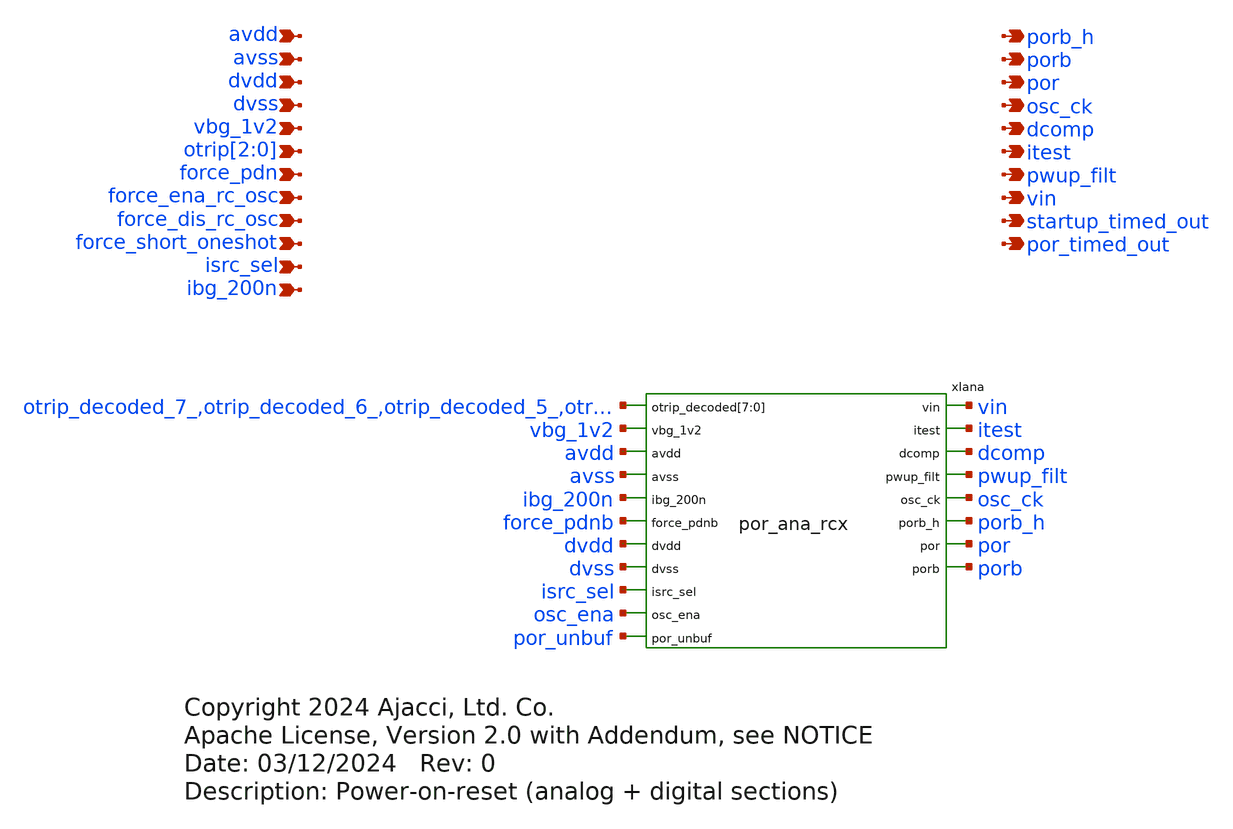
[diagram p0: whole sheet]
** sch_path: xschem/sky130_ajc_ip__por.sch
* Copyright 2024 Ajacci, Ltd. Co.
* Apache License, Version 2.0 with Addendum, see NOTICE
**.subckt sky130_ajc_ip__por avdd avss dvdd dvss vbg_1v2 otrip[2],otrip[1],otrip[0] force_pdn
*+ force_ena_rc_osc force_short_oneshot isrc_sel ibg_200n vin porb_h porb por osc_ck pwup_filt itest startup_timed_out
*+ por_timed_out force_dis_rc_osc dcomp
*.ipin avdd
*.ipin avss
*.ipin dvdd
*.ipin dvss
*.ipin vbg_1v2
*.ipin otrip[2],otrip[1],otrip[0]
*.ipin force_pdn
*.ipin force_ena_rc_osc
*.ipin force_short_oneshot
*.ipin isrc_sel
*.ipin ibg_200n
*.opin vin
*.opin porb_h
*.opin porb
*.opin por
*.opin osc_ck
*.opin pwup_filt
*.opin itest
*.opin startup_timed_out
*.opin por_timed_out
*.ipin force_dis_rc_osc
*.opin dcomp
xIana vin otrip_decoded_7_ otrip_decoded_6_ otrip_decoded_5_ otrip_decoded_4_ otrip_decoded_3_
+ otrip_decoded_2_ otrip_decoded_1_ otrip_decoded_0_ vbg_1v2 avdd itest avss ibg_200n force_pdnb dvdd dvss dcomp
+ isrc_sel pwup_filt osc_ck osc_ena porb_h por_unbuf por porb por_ana_rcx
**** begin user architecture code



r0 otrip[0] otrip0 1
r1 otrip[1] otrip1 1
r2 otrip[2] otrip2 1

*XSPICE CO-SIM netlist
.include por_dig.out.spice
xipor_dig dvss dvdd force_dis_rc_osc force_ena_rc_osc force_pdn force_pdnb force_short_oneshot
+ osc_ck osc_ena  otrip0 otrip1 otrip2 otrip_decoded_0_ otrip_decoded_1_ otrip_decoded_2_ otrip_decoded_3_
+ otrip_decoded_4_ otrip_decoded_5_ otrip_decoded_6_ otrip_decoded_7_ por_timed_out por_unbuf pwup_filt
+ startup_timed_out por_dig


**** end user architecture code
**.ends

* expanding   symbol:  xschem/por_ana_rcx.sym # of pins=19
** sym_path: xschem/por_ana_rcx.sym
** sch_path: xschem/por_ana_rcx.sch
.subckt por_ana_rcx vin otrip_decoded[7] otrip_decoded[6] otrip_decoded[5] otrip_decoded[4]
+ otrip_decoded[3] otrip_decoded[2] otrip_decoded[1] otrip_decoded[0] vbg_1v2 avdd itest avss ibg_200n force_pdnb dvdd
+ dvss dcomp isrc_sel pwup_filt osc_ck osc_ena porb_h por_unbuf por porb
*.ipin vbg_1v2
*.ipin avdd
*.ipin avss
*.ipin dvdd
*.ipin dvss
*.ipin force_pdnb
*.ipin isrc_sel
*.ipin ibg_200n
*.opin pwup_filt
*.opin itest
*.ipin osc_ena
*.opin osc_ck
*.ipin
*+ otrip_decoded[7],otrip_decoded[6],otrip_decoded[5],otrip_decoded[4],otrip_decoded[3],otrip_decoded[2],otrip_decoded[1],otrip_decoded[0]
*.opin vin
*.ipin por_unbuf
*.opin porb_h
*.opin por
*.opin porb
*.opin dcomp
**** begin user architecture code



.include mag/rcx/por_ana_rcx.spice

xIana vin otrip_decoded[7] otrip_decoded[6] otrip_decoded[5] otrip_decoded[4]  otrip_decoded[3]
+ otrip_decoded[2] otrip_decoded[1] otrip_decoded[0] vbg_1v2 avdd itest avss ibg_200n force_pdnb dvdd dvss dcomp
+ isrc_sel pwup_filt osc_ck osc_ena porb_h por_unbuf por porb por_ana



**** end user architecture code
.ends

.end
